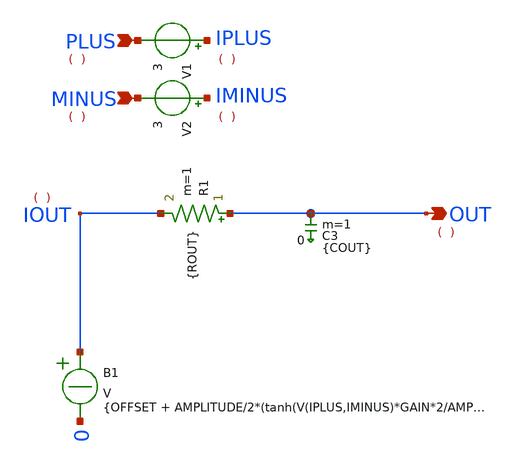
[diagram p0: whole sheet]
** sch_path: Behavioral_model/comp_behavioral.sch
**.subckt comp_behavioral PLUS MINUS OUT
*.ipin PLUS
*.ipin MINUS
*.opin OUT
B1 IOUT 0 V = {OFFSET + AMPLITUDE/2*(tanh(V(IPLUS,IMINUS)*GAIN*2/AMPLITUDE))}
V1 IPLUS PLUS 3
V2 IMINUS MINUS 3
R1 OUT IOUT {ROUT} m=1
C3 OUT 0 {COUT} m=1
**.ends
.end
